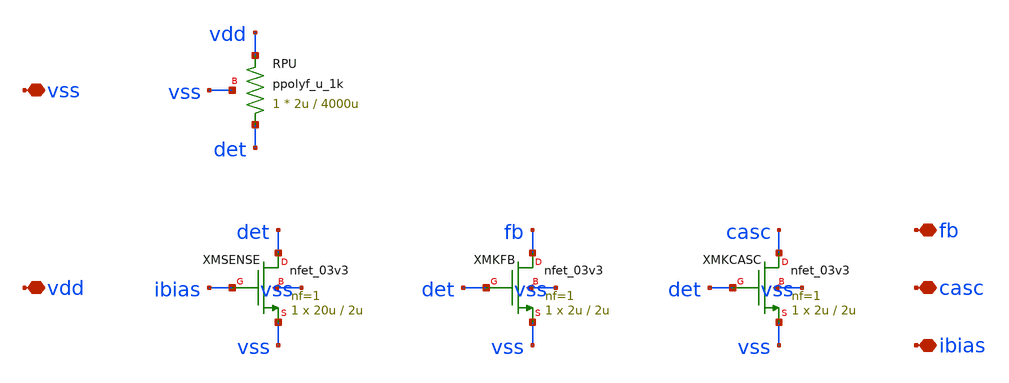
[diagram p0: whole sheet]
** sch_path: design/bandgap_startup.sch
**.subckt bandgap_startup vdd vss fb casc ibias
*.iopin vdd
*.iopin vss
*.iopin fb
*.iopin casc
*.iopin ibias
XMSENSE det ibias vss vss nfet_03v3 L=2u W=20u nf=1 ad='int((nf+1)/2) * W/nf * 0.18u' as='int((nf+2)/2) * W/nf * 0.18u'
+ pd='2*int((nf+1)/2) * (W/nf + 0.18u)' ps='2*int((nf+2)/2) * (W/nf + 0.18u)' nrd='0.18u / W' nrs='0.18u / W'
+ sa=0 sb=0 sd=0 m=1
XRPU det vdd vss ppolyf_u_1k r_width=2u r_length=4000u m=1
XMKFB fb det vss vss nfet_03v3 L=2u W=2u nf=1 ad='int((nf+1)/2) * W/nf * 0.18u' as='int((nf+2)/2) * W/nf * 0.18u'
+ pd='2*int((nf+1)/2) * (W/nf + 0.18u)' ps='2*int((nf+2)/2) * (W/nf + 0.18u)' nrd='0.18u / W' nrs='0.18u / W'
+ sa=0 sb=0 sd=0 m=1
XMKCASC casc det vss vss nfet_03v3 L=2u W=2u nf=1 ad='int((nf+1)/2) * W/nf * 0.18u' as='int((nf+2)/2) * W/nf * 0.18u'
+ pd='2*int((nf+1)/2) * (W/nf + 0.18u)' ps='2*int((nf+2)/2) * (W/nf + 0.18u)' nrd='0.18u / W' nrs='0.18u / W'
+ sa=0 sb=0 sd=0 m=1
**.ends
.end
